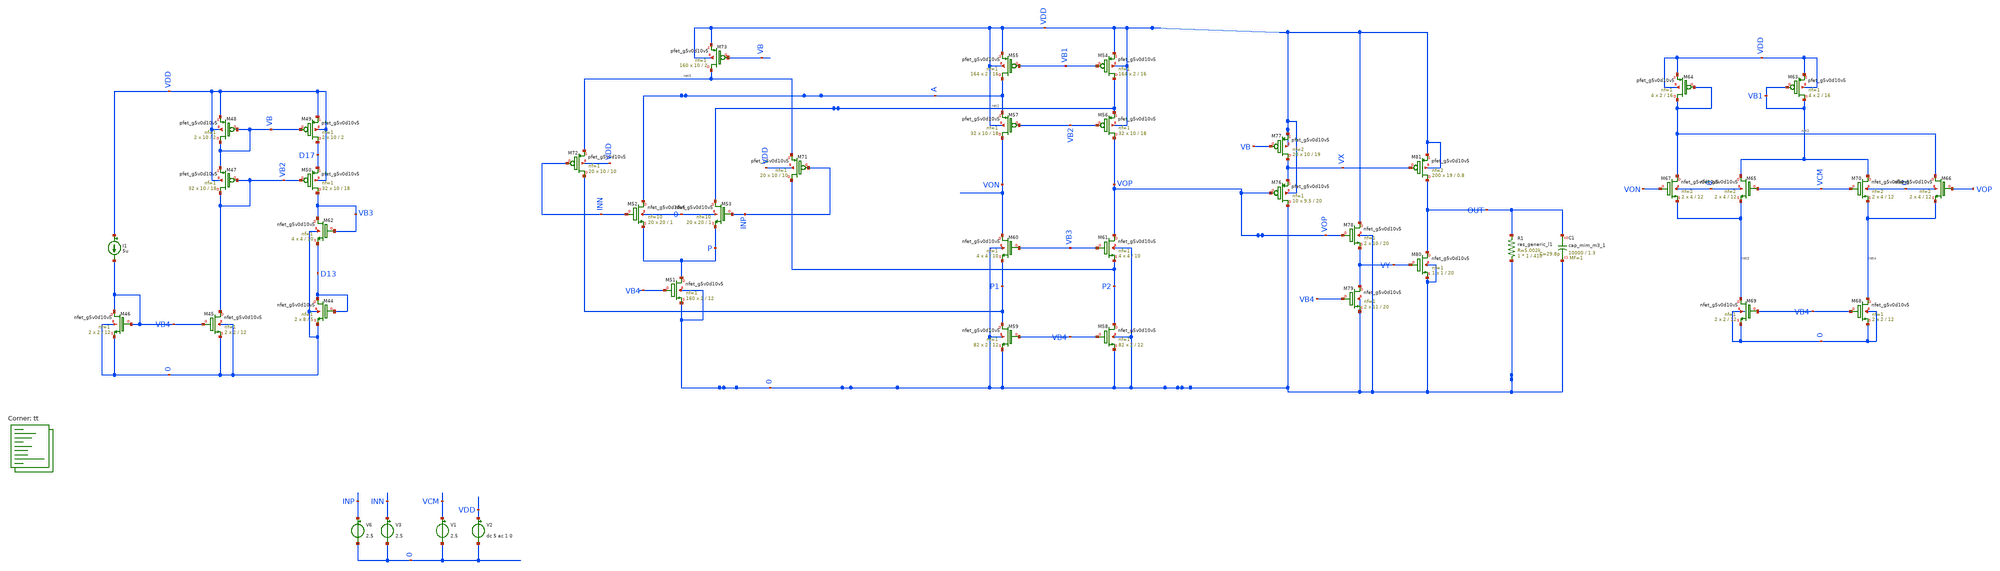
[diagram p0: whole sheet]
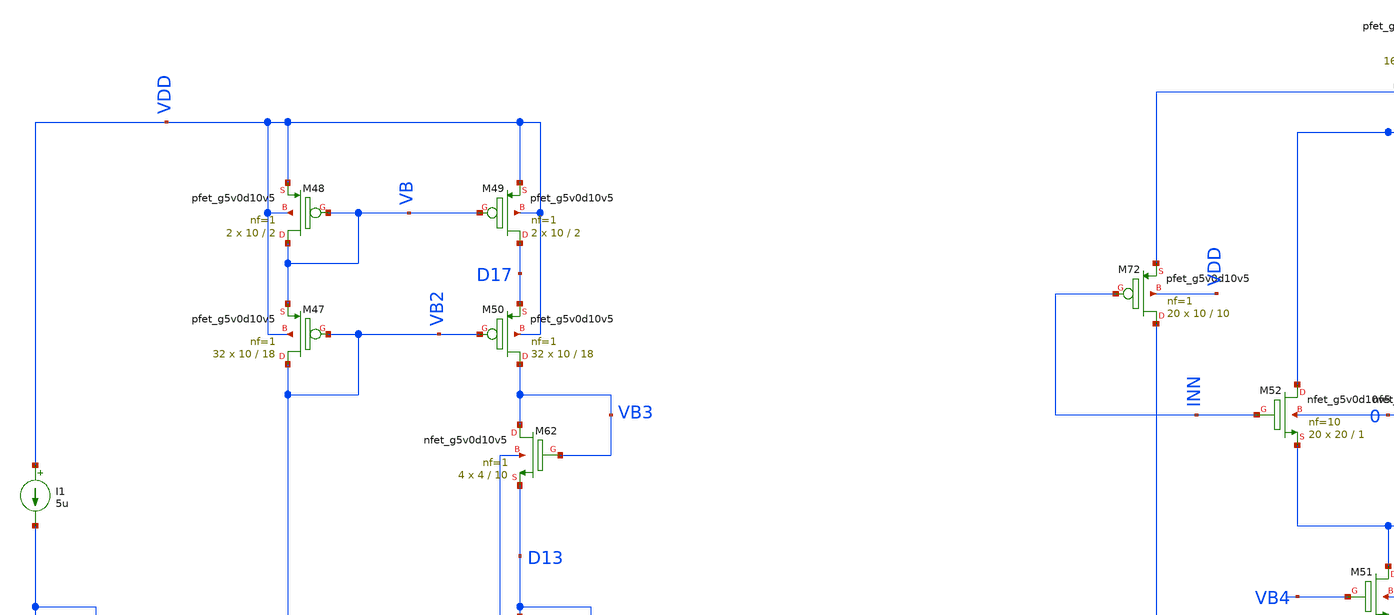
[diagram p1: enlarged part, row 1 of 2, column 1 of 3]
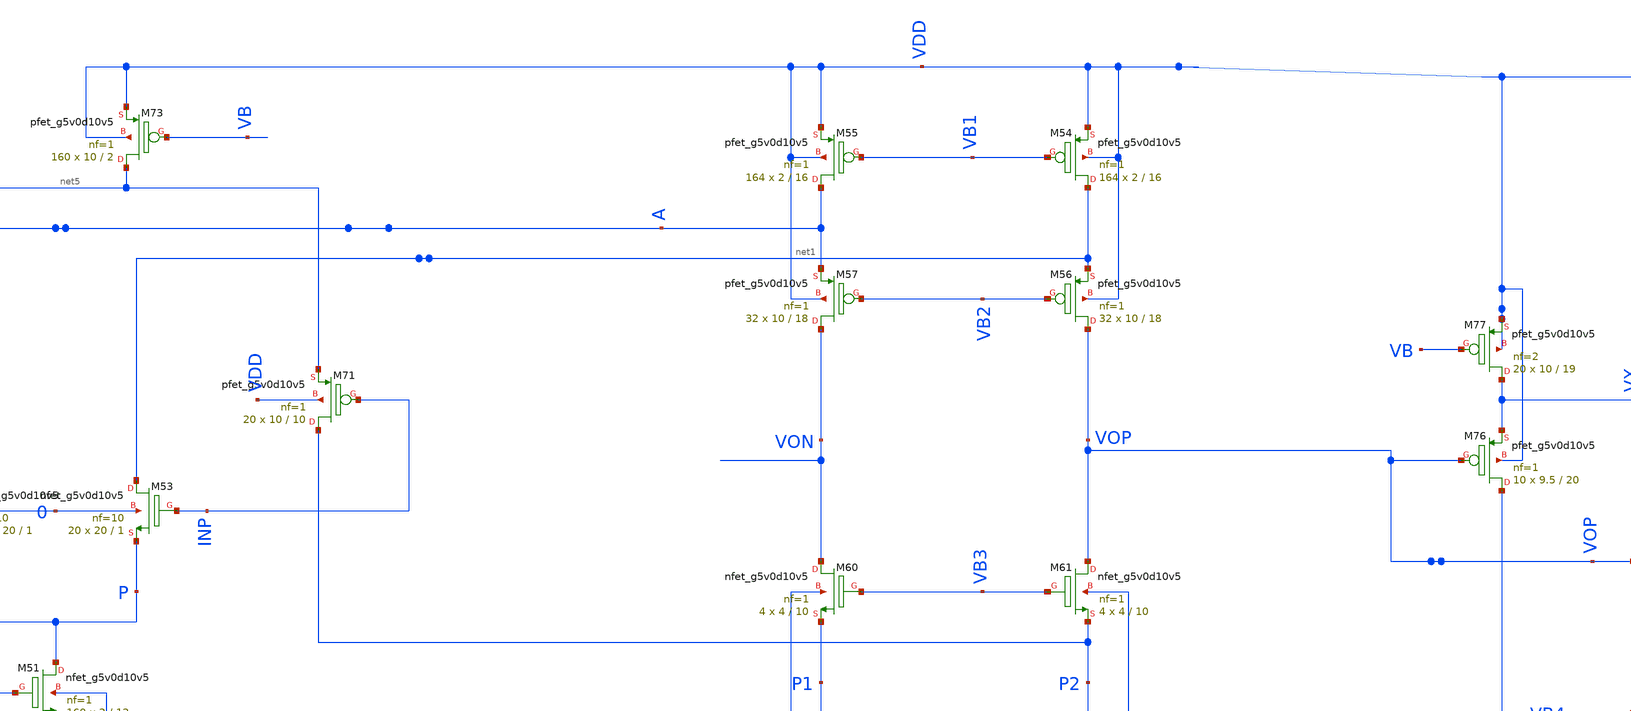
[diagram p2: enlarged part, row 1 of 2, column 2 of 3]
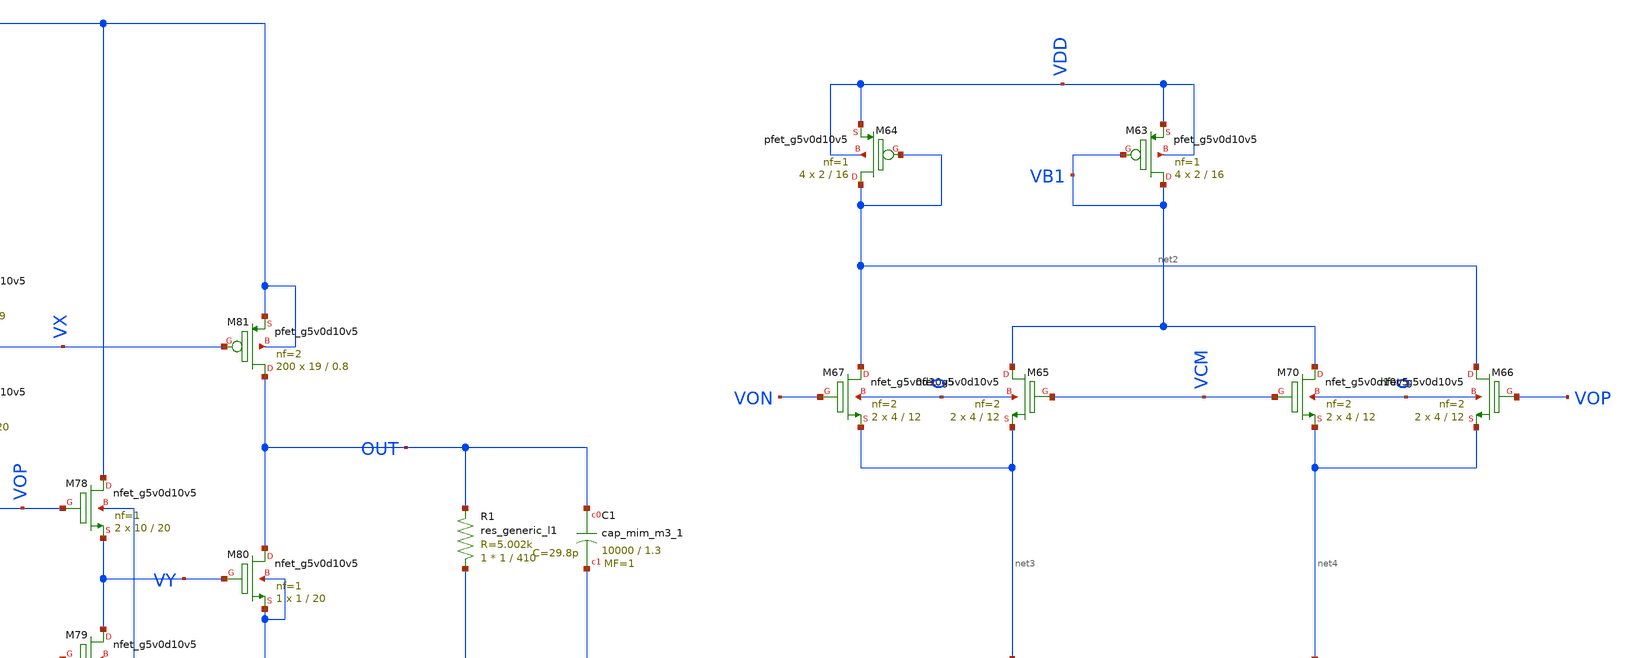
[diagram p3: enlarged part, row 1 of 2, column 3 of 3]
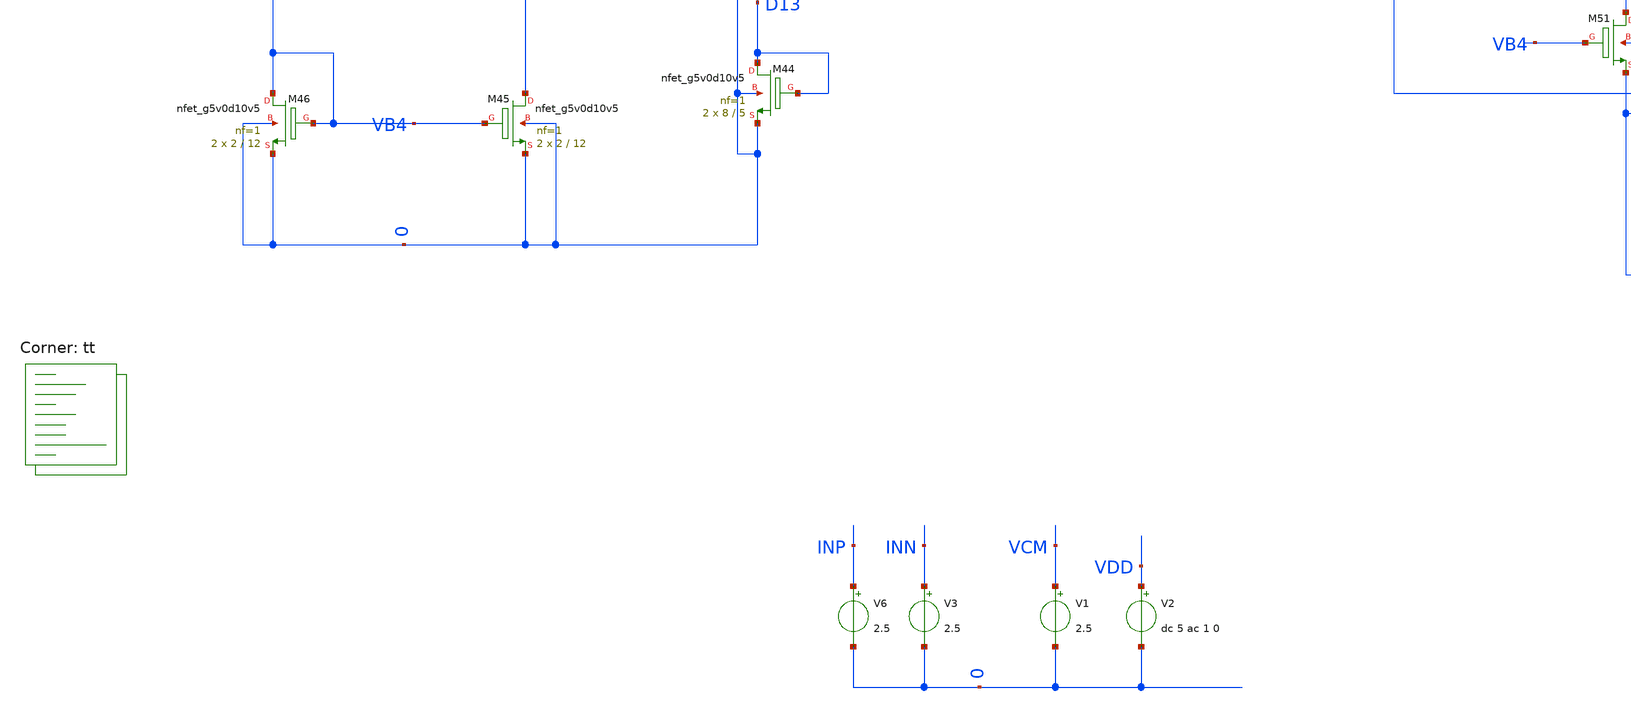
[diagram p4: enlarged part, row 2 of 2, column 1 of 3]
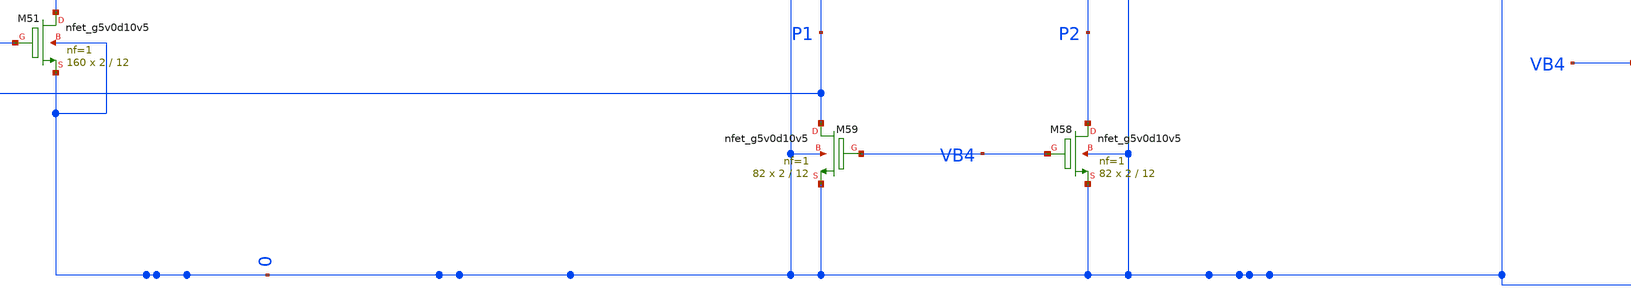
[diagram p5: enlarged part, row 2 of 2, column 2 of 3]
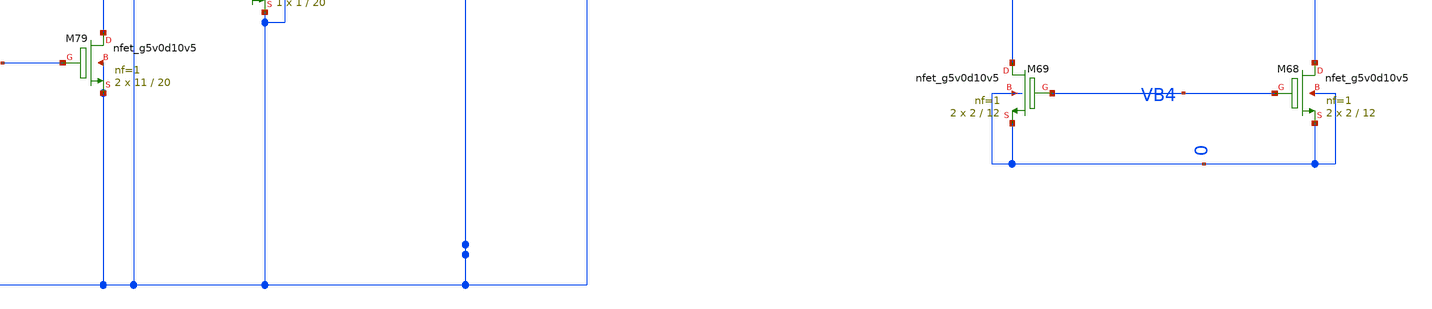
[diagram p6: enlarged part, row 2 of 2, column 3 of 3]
** sch_path: Xschem_UPDATE/tb_PSRR_MEAS_final.sch
**.subckt tb_PSRR_MEAS_final
V6 INP 0 2.5
V1 VCM 0 2.5
V2 VDD 0 dc 5 ac 1 0
V3 INN 0 2.5
I1 VDD VB4 5u
XM44 D13 D13 0 0 sky130_fd_pr__nfet_g5v0d10v5 L=5 W=8 nf=1 ad='int((nf+1)/2) * W/nf * 0.29' as='int((nf+2)/2) * W/nf * 0.29'
+ pd='2*int((nf+1)/2) * (W/nf + 0.29)' ps='2*int((nf+2)/2) * (W/nf + 0.29)' nrd='0.29 / W' nrs='0.29 / W'
+ sa=0 sb=0 sd=0 mult=2 m=2
XM45 VB2 VB4 0 0 sky130_fd_pr__nfet_g5v0d10v5 L=12 W=2 nf=1 ad='int((nf+1)/2) * W/nf * 0.29' as='int((nf+2)/2) * W/nf * 0.29'
+ pd='2*int((nf+1)/2) * (W/nf + 0.29)' ps='2*int((nf+2)/2) * (W/nf + 0.29)' nrd='0.29 / W' nrs='0.29 / W'
+ sa=0 sb=0 sd=0 mult=2 m=2
XM46 VB4 VB4 0 0 sky130_fd_pr__nfet_g5v0d10v5 L=12 W=2 nf=1 ad='int((nf+1)/2) * W/nf * 0.29' as='int((nf+2)/2) * W/nf * 0.29'
+ pd='2*int((nf+1)/2) * (W/nf + 0.29)' ps='2*int((nf+2)/2) * (W/nf + 0.29)' nrd='0.29 / W' nrs='0.29 / W'
+ sa=0 sb=0 sd=0 mult=2 m=2
XM47 VB2 VB2 VB VDD sky130_fd_pr__pfet_g5v0d10v5 L=18 W=10 nf=1 ad='int((nf+1)/2) * W/nf * 0.29' as='int((nf+2)/2) * W/nf * 0.29'
+ pd='2*int((nf+1)/2) * (W/nf + 0.29)' ps='2*int((nf+2)/2) * (W/nf + 0.29)' nrd='0.29 / W' nrs='0.29 / W'
+ sa=0 sb=0 sd=0 mult=32 m=32
XM48 VB VB VDD VDD sky130_fd_pr__pfet_g5v0d10v5 L=2 W=10 nf=1 ad='int((nf+1)/2) * W/nf * 0.29' as='int((nf+2)/2) * W/nf * 0.29'
+ pd='2*int((nf+1)/2) * (W/nf + 0.29)' ps='2*int((nf+2)/2) * (W/nf + 0.29)' nrd='0.29 / W' nrs='0.29 / W'
+ sa=0 sb=0 sd=0 mult=2 m=2
XM49 D17 VB VDD VDD sky130_fd_pr__pfet_g5v0d10v5 L=2 W=10 nf=1 ad='int((nf+1)/2) * W/nf * 0.29' as='int((nf+2)/2) * W/nf * 0.29'
+ pd='2*int((nf+1)/2) * (W/nf + 0.29)' ps='2*int((nf+2)/2) * (W/nf + 0.29)' nrd='0.29 / W' nrs='0.29 / W'
+ sa=0 sb=0 sd=0 mult=2 m=2
XM50 VB3 VB2 D17 VDD sky130_fd_pr__pfet_g5v0d10v5 L=18 W=10 nf=1 ad='int((nf+1)/2) * W/nf * 0.29' as='int((nf+2)/2) * W/nf * 0.29'
+ pd='2*int((nf+1)/2) * (W/nf + 0.29)' ps='2*int((nf+2)/2) * (W/nf + 0.29)' nrd='0.29 / W' nrs='0.29 / W'
+ sa=0 sb=0 sd=0 mult=32 m=32
XM51 P VB4 0 0 sky130_fd_pr__nfet_g5v0d10v5 L=12 W=2 nf=1 ad='int((nf+1)/2) * W/nf * 0.29' as='int((nf+2)/2) * W/nf * 0.29'
+ pd='2*int((nf+1)/2) * (W/nf + 0.29)' ps='2*int((nf+2)/2) * (W/nf + 0.29)' nrd='0.29 / W' nrs='0.29 / W'
+ sa=0 sb=0 sd=0 mult=160 m=160
XM52 A INN P 0 sky130_fd_pr__nfet_g5v0d10v5 L=1 W=20 nf=10 ad='int((nf+1)/2) * W/nf * 0.29' as='int((nf+2)/2) * W/nf * 0.29'
+ pd='2*int((nf+1)/2) * (W/nf + 0.29)' ps='2*int((nf+2)/2) * (W/nf + 0.29)' nrd='0.29 / W' nrs='0.29 / W'
+ sa=0 sb=0 sd=0 mult=20 m=20
XM53 net1 INP P 0 sky130_fd_pr__nfet_g5v0d10v5 L=1 W=20 nf=10 ad='int((nf+1)/2) * W/nf * 0.29' as='int((nf+2)/2) * W/nf * 0.29'
+ pd='2*int((nf+1)/2) * (W/nf + 0.29)' ps='2*int((nf+2)/2) * (W/nf + 0.29)' nrd='0.29 / W' nrs='0.29 / W'
+ sa=0 sb=0 sd=0 mult=20 m=20
XM54 net1 VB1 VDD VDD sky130_fd_pr__pfet_g5v0d10v5 L=16 W=2 nf=1 ad='int((nf+1)/2) * W/nf * 0.29' as='int((nf+2)/2) * W/nf * 0.29'
+ pd='2*int((nf+1)/2) * (W/nf + 0.29)' ps='2*int((nf+2)/2) * (W/nf + 0.29)' nrd='0.29 / W' nrs='0.29 / W'
+ sa=0 sb=0 sd=0 mult=164 m=164
XM55 A VB1 VDD VDD sky130_fd_pr__pfet_g5v0d10v5 L=16 W=2 nf=1 ad='int((nf+1)/2) * W/nf * 0.29' as='int((nf+2)/2) * W/nf * 0.29'
+ pd='2*int((nf+1)/2) * (W/nf + 0.29)' ps='2*int((nf+2)/2) * (W/nf + 0.29)' nrd='0.29 / W' nrs='0.29 / W'
+ sa=0 sb=0 sd=0 mult=164 m=164
XM56 VOP VB2 net1 VDD sky130_fd_pr__pfet_g5v0d10v5 L=18 W=10 nf=1 ad='int((nf+1)/2) * W/nf * 0.29' as='int((nf+2)/2) * W/nf * 0.29'
+ pd='2*int((nf+1)/2) * (W/nf + 0.29)' ps='2*int((nf+2)/2) * (W/nf + 0.29)' nrd='0.29 / W' nrs='0.29 / W'
+ sa=0 sb=0 sd=0 mult=32 m=32
XM57 VON VB2 A VDD sky130_fd_pr__pfet_g5v0d10v5 L=18 W=10 nf=1 ad='int((nf+1)/2) * W/nf * 0.29' as='int((nf+2)/2) * W/nf * 0.29'
+ pd='2*int((nf+1)/2) * (W/nf + 0.29)' ps='2*int((nf+2)/2) * (W/nf + 0.29)' nrd='0.29 / W' nrs='0.29 / W'
+ sa=0 sb=0 sd=0 mult=32 m=32
XM58 P2 VB4 0 0 sky130_fd_pr__nfet_g5v0d10v5 L=12 W=2 nf=1 ad='int((nf+1)/2) * W/nf * 0.29' as='int((nf+2)/2) * W/nf * 0.29'
+ pd='2*int((nf+1)/2) * (W/nf + 0.29)' ps='2*int((nf+2)/2) * (W/nf + 0.29)' nrd='0.29 / W' nrs='0.29 / W'
+ sa=0 sb=0 sd=0 mult=82 m=82
XM59 P1 VB4 0 0 sky130_fd_pr__nfet_g5v0d10v5 L=12 W=2 nf=1 ad='int((nf+1)/2) * W/nf * 0.29' as='int((nf+2)/2) * W/nf * 0.29'
+ pd='2*int((nf+1)/2) * (W/nf + 0.29)' ps='2*int((nf+2)/2) * (W/nf + 0.29)' nrd='0.29 / W' nrs='0.29 / W'
+ sa=0 sb=0 sd=0 mult=82 m=82
XM60 VON VB3 P1 0 sky130_fd_pr__nfet_g5v0d10v5 L=10 W=4 nf=1 ad='int((nf+1)/2) * W/nf * 0.29' as='int((nf+2)/2) * W/nf * 0.29'
+ pd='2*int((nf+1)/2) * (W/nf + 0.29)' ps='2*int((nf+2)/2) * (W/nf + 0.29)' nrd='0.29 / W' nrs='0.29 / W'
+ sa=0 sb=0 sd=0 mult=4 m=4
XM61 VOP VB3 P2 0 sky130_fd_pr__nfet_g5v0d10v5 L=10 W=4 nf=1 ad='int((nf+1)/2) * W/nf * 0.29' as='int((nf+2)/2) * W/nf * 0.29'
+ pd='2*int((nf+1)/2) * (W/nf + 0.29)' ps='2*int((nf+2)/2) * (W/nf + 0.29)' nrd='0.29 / W' nrs='0.29 / W'
+ sa=0 sb=0 sd=0 mult=4 m=4
XM62 VB3 VB3 D13 0 sky130_fd_pr__nfet_g5v0d10v5 L=10 W=4 nf=1 ad='int((nf+1)/2) * W/nf * 0.29' as='int((nf+2)/2) * W/nf * 0.29'
+ pd='2*int((nf+1)/2) * (W/nf + 0.29)' ps='2*int((nf+2)/2) * (W/nf + 0.29)' nrd='0.29 / W' nrs='0.29 / W'
+ sa=0 sb=0 sd=0 mult=4 m=4
XM63 VB1 VB1 VDD VDD sky130_fd_pr__pfet_g5v0d10v5 L=16 W=2 nf=1 ad='int((nf+1)/2) * W/nf * 0.29' as='int((nf+2)/2) * W/nf * 0.29'
+ pd='2*int((nf+1)/2) * (W/nf + 0.29)' ps='2*int((nf+2)/2) * (W/nf + 0.29)' nrd='0.29 / W' nrs='0.29 / W'
+ sa=0 sb=0 sd=0 mult=4 m=4
XM64 net2 net2 VDD VDD sky130_fd_pr__pfet_g5v0d10v5 L=16 W=2 nf=1 ad='int((nf+1)/2) * W/nf * 0.29' as='int((nf+2)/2) * W/nf * 0.29'
+ pd='2*int((nf+1)/2) * (W/nf + 0.29)' ps='2*int((nf+2)/2) * (W/nf + 0.29)' nrd='0.29 / W' nrs='0.29 / W'
+ sa=0 sb=0 sd=0 mult=4 m=4
XM65 VB1 VCM net3 0 sky130_fd_pr__nfet_g5v0d10v5 L=12 W=4 nf=2 ad='int((nf+1)/2) * W/nf * 0.29' as='int((nf+2)/2) * W/nf * 0.29'
+ pd='2*int((nf+1)/2) * (W/nf + 0.29)' ps='2*int((nf+2)/2) * (W/nf + 0.29)' nrd='0.29 / W' nrs='0.29 / W'
+ sa=0 sb=0 sd=0 mult=2 m=2
XM66 net2 VOP net4 0 sky130_fd_pr__nfet_g5v0d10v5 L=12 W=4 nf=2 ad='int((nf+1)/2) * W/nf * 0.29' as='int((nf+2)/2) * W/nf * 0.29'
+ pd='2*int((nf+1)/2) * (W/nf + 0.29)' ps='2*int((nf+2)/2) * (W/nf + 0.29)' nrd='0.29 / W' nrs='0.29 / W'
+ sa=0 sb=0 sd=0 mult=2 m=2
XM67 net2 VON net3 0 sky130_fd_pr__nfet_g5v0d10v5 L=12 W=4 nf=2 ad='int((nf+1)/2) * W/nf * 0.29' as='int((nf+2)/2) * W/nf * 0.29'
+ pd='2*int((nf+1)/2) * (W/nf + 0.29)' ps='2*int((nf+2)/2) * (W/nf + 0.29)' nrd='0.29 / W' nrs='0.29 / W'
+ sa=0 sb=0 sd=0 mult=2 m=2
XM68 net4 VB4 0 0 sky130_fd_pr__nfet_g5v0d10v5 L=12 W=2 nf=1 ad='int((nf+1)/2) * W/nf * 0.29' as='int((nf+2)/2) * W/nf * 0.29'
+ pd='2*int((nf+1)/2) * (W/nf + 0.29)' ps='2*int((nf+2)/2) * (W/nf + 0.29)' nrd='0.29 / W' nrs='0.29 / W'
+ sa=0 sb=0 sd=0 mult=2 m=2
XM69 net3 VB4 0 0 sky130_fd_pr__nfet_g5v0d10v5 L=12 W=2 nf=1 ad='int((nf+1)/2) * W/nf * 0.29' as='int((nf+2)/2) * W/nf * 0.29'
+ pd='2*int((nf+1)/2) * (W/nf + 0.29)' ps='2*int((nf+2)/2) * (W/nf + 0.29)' nrd='0.29 / W' nrs='0.29 / W'
+ sa=0 sb=0 sd=0 mult=2 m=2
XM70 VB1 VCM net4 0 sky130_fd_pr__nfet_g5v0d10v5 L=12 W=4 nf=2 ad='int((nf+1)/2) * W/nf * 0.29' as='int((nf+2)/2) * W/nf * 0.29'
+ pd='2*int((nf+1)/2) * (W/nf + 0.29)' ps='2*int((nf+2)/2) * (W/nf + 0.29)' nrd='0.29 / W' nrs='0.29 / W'
+ sa=0 sb=0 sd=0 mult=2 m=2
XM71 P2 INP net5 VDD sky130_fd_pr__pfet_g5v0d10v5 L=10 W=10 nf=1 ad='int((nf+1)/2) * W/nf * 0.29' as='int((nf+2)/2) * W/nf * 0.29'
+ pd='2*int((nf+1)/2) * (W/nf + 0.29)' ps='2*int((nf+2)/2) * (W/nf + 0.29)' nrd='0.29 / W' nrs='0.29 / W'
+ sa=0 sb=0 sd=0 mult=20 m=20
XM72 P1 INN net5 VDD sky130_fd_pr__pfet_g5v0d10v5 L=10 W=10 nf=1 ad='int((nf+1)/2) * W/nf * 0.29' as='int((nf+2)/2) * W/nf * 0.29'
+ pd='2*int((nf+1)/2) * (W/nf + 0.29)' ps='2*int((nf+2)/2) * (W/nf + 0.29)' nrd='0.29 / W' nrs='0.29 / W'
+ sa=0 sb=0 sd=0 mult=20 m=20
XM73 net5 VB VDD VDD sky130_fd_pr__pfet_g5v0d10v5 L=2 W=10 nf=1 ad='int((nf+1)/2) * W/nf * 0.29' as='int((nf+2)/2) * W/nf * 0.29'
+ pd='2*int((nf+1)/2) * (W/nf + 0.29)' ps='2*int((nf+2)/2) * (W/nf + 0.29)' nrd='0.29 / W' nrs='0.29 / W'
+ sa=0 sb=0 sd=0 mult=160 m=160
XM76 0 VOP VX VDD sky130_fd_pr__pfet_g5v0d10v5 L=20 W=9.5 nf=1 ad='int((nf+1)/2) * W/nf * 0.29' as='int((nf+2)/2) * W/nf * 0.29'
+ pd='2*int((nf+1)/2) * (W/nf + 0.29)' ps='2*int((nf+2)/2) * (W/nf + 0.29)' nrd='0.29 / W' nrs='0.29 / W'
+ sa=0 sb=0 sd=0 mult=10 m=10
XM77 VX VB VDD VDD sky130_fd_pr__pfet_g5v0d10v5 L=19 W=10 nf=2 ad='int((nf+1)/2) * W/nf * 0.29' as='int((nf+2)/2) * W/nf * 0.29'
+ pd='2*int((nf+1)/2) * (W/nf + 0.29)' ps='2*int((nf+2)/2) * (W/nf + 0.29)' nrd='0.29 / W' nrs='0.29 / W'
+ sa=0 sb=0 sd=0 mult=20 m=20
XM78 VDD VOP VY 0 sky130_fd_pr__nfet_g5v0d10v5 L=20 W=10 nf=1 ad='int((nf+1)/2) * W/nf * 0.29' as='int((nf+2)/2) * W/nf * 0.29'
+ pd='2*int((nf+1)/2) * (W/nf + 0.29)' ps='2*int((nf+2)/2) * (W/nf + 0.29)' nrd='0.29 / W' nrs='0.29 / W'
+ sa=0 sb=0 sd=0 mult=2 m=2
XM79 VY VB4 0 0 sky130_fd_pr__nfet_g5v0d10v5 L=20 W=11 nf=1 ad='int((nf+1)/2) * W/nf * 0.29' as='int((nf+2)/2) * W/nf * 0.29'
+ pd='2*int((nf+1)/2) * (W/nf + 0.29)' ps='2*int((nf+2)/2) * (W/nf + 0.29)' nrd='0.29 / W' nrs='0.29 / W'
+ sa=0 sb=0 sd=0 mult=2 m=2
XM80 OUT VY 0 0 sky130_fd_pr__nfet_g5v0d10v5 L=20 W=1 nf=1 ad='int((nf+1)/2) * W/nf * 0.29' as='int((nf+2)/2) * W/nf * 0.29'
+ pd='2*int((nf+1)/2) * (W/nf + 0.29)' ps='2*int((nf+2)/2) * (W/nf + 0.29)' nrd='0.29 / W' nrs='0.29 / W'
+ sa=0 sb=0 sd=0 mult=1 m=1
XM81 OUT VX VDD VDD sky130_fd_pr__pfet_g5v0d10v5 L=0.8 W=19 nf=2 ad='int((nf+1)/2) * W/nf * 0.29' as='int((nf+2)/2) * W/nf * 0.29'
+ pd='2*int((nf+1)/2) * (W/nf + 0.29)' ps='2*int((nf+2)/2) * (W/nf + 0.29)' nrd='0.29 / W' nrs='0.29 / W'
+ sa=0 sb=0 sd=0 mult=200 m=200
XC1 OUT 0 sky130_fd_pr__cap_mim_m3_1 W=10000 L=1.3 MF=1 m=1
R1 0 OUT sky130_fd_pr__res_generic_l1 W=1 L=410 m=1
**** begin user architecture code

* this option enables mos model bin
* selection based on W/NF instead of W
.option wnflag=1
.option savecurrents

.control
save all
save @m.xm15.msky130_fd_pr__pfet_g5v0d10v5[vth]
save @m.xm15.msky130_fd_pr__pfet_g5v0d10v5[gm]
save @m.xm9.msky130_fd_pr__pfet_g5v0d10v5[vth]
save @m.xm9.msky130_fd_pr__pfet_g5v0d10v5[gm]
save @m.xm8.msky130_fd_pr__pfet_g5v0d10v5[vth]
save @m.xm8.msky130_fd_pr__pfet_g5v0d10v5[gm]
save @m.xm20.msky130_fd_pr__pfet_g5v0d10v5[vth]
save @m.xm20.msky130_fd_pr__pfet_g5v0d10v5[gm]
save @m.xm7.msky130_fd_pr__pfet_g5v0d10v5[vth]
save @m.xm7.msky130_fd_pr__pfet_g5v0d10v5[gm]
save @m.xm10.msky130_fd_pr__nfet_g5v0d10v5[gm]
save @m.xm10.msky130_fd_pr__nfet_g5v0d10v5[vth]
save @m.xm14.msky130_fd_pr__pfet_g5v0d10v5[gm]
save @m.xm14.msky130_fd_pr__pfet_g5v0d10v5[vth]
save @m.xm16.msky130_fd_pr__pfet_g5v0d10v5[gm]
save @m.xm16.msky130_fd_pr__pfet_g5v0d10v5[vth]
save @m.xm17.msky130_fd_pr__pfet_g5v0d10v5[gm]
save @m.xm17.msky130_fd_pr__pfet_g5v0d10v5[vth]
save @m.xm13.msky130_fd_pr__nfet_g5v0d10v5[gm]
save @m.xm13.msky130_fd_pr__nfet_g5v0d10v5[vth]
save @m.xm12.msky130_fd_pr__nfet_g5v0d10v5[vth]
save @m.xm18.msky130_fd_pr__nfet_g5v0d10v5[vth]
*folded
save @m.xm2.msky130_fd_pr__nfet_g5v0d10v5[vth]
save @m.xm11.msky130_fd_pr__nfet_g5v0d10v5[vth]
save @m.xm1.msky130_fd_pr__nfet_g5v0d10v5[vth]
save @m.xm5.msky130_fd_pr__nfet_g5v0d10v5[vth]
save @m.xm6.msky130_fd_pr__nfet_g5v0d10v5[vth]
save @m.xm4.msky130_fd_pr__nfet_g5v0d10v5[vth]
save @m.xm3.msky130_fd_pr__nfet_g5v0d10v5[vth]
save @m.xm7.msky130_fd_pr__pfet_g5v0d10v5[vth]
save @m.xm8.msky130_fd_pr__pfet_g5v0d10v5[vth]
save @m.xm9.msky130_fd_pr__pfet_g5v0d10v5[vth]
save @m.xm20.msky130_fd_pr__pfet_g5v0d10v5[vth]
*CMFB
save @m.xm21.msky130_fd_pr__pfet_g5v0d10v5[vth]
save @m.xm19.msky130_fd_pr__pfet_g5v0d10v5[vth]
save @m.xm22.msky130_fd_pr__nfet_g5v0d10v5[vth]
save @m.xm23.msky130_fd_pr__nfet_g5v0d10v5[vth]
save @m.xm25.msky130_fd_pr__nfet_g5v0d10v5[vth]
save @m.xm27.msky130_fd_pr__nfet_g5v0d10v5[vth]
save @m.xm26.msky130_fd_pr__nfet_g5v0d10v5[vth]
save @m.xm24.msky130_fd_pr__nfet_g5v0d10v5[vth]
save current


write Folded_Buffer.raw

op
print VON VOP VB2 VB VX OUT VY
*print @m.xm18.msky130_fd_pr__nfet_g5v0d10v5
*print @m.xm12.msky130_fd_pr__nfet_g5v0d10v5
*print @m.xm13.msky130_fd_pr__nfet_g5v0d10v5
*print @m.xm10.msky130_fd_pr__nfet_g5v0d10v5
*print @m.xm14.msky130_fd_pr__pfet_g5v0d10v5
*print @m.xm17.msky130_fd_pr__pfet_g5v0d10v5
*print @m.xm15.msky130_fd_pr__pfet_g5v0d10v5
*print @m.xm16.msky130_fd_pr__pfet_g5v0d10v5
*Folded cascode
*print @m.xm9.msky130_fd_pr__pfet_g5v0d10v5
*print @m.xm8.msky130_fd_pr__pfet_g5v0d10v5
*print @m.xm5.msky130_fd_pr__nfet_g5v0d10v5
*print @m.xm4.msky130_fd_pr__nfet_g5v0d10v5
*print @m.xm1.msky130_fd_pr__nfet_g5v0d10v5
*print @m.xm2.msky130_fd_pr__nfet_g5v0d10v5
*print @m.xm11.msky130_fd_pr__nfet_g5v0d10v5
*CMFB
*print @m.xm23.msky130_fd_pr__nfet_g5v0d10v5
*print @m.xm24.msky130_fd_pr__nfet_g5v0d10v5
*print @m.xm25.msky130_fd_pr__nfet_g5v0d10v5
*print @m.xm22.msky130_fd_pr__nfet_g5v0d10v5
print @m.xm77.msky130_fd_pr__pfet_g5v0d10v5
print @m.xm76.msky130_fd_pr__pfet_g5v0d10v5
print @m.xm78.msky130_fd_pr__nfet_g5v0d10v5
print @m.xm79.msky130_fd_pr__nfet_g5v0d10v5
print @m.xm80.msky130_fd_pr__nfet_g5v0d10v5
print @m.xm81.msky130_fd_pr__pfet_g5v0d10v5
write Folded_Buffer.raw
ac dec 10 1 1e9
  remzerovec
  write tb_PSRR_MEAS_final.raw
quit 0
.endc


.lib $::SKYWATER_MODELS/sky130.lib.spice tt
**** end user architecture code
**.ends
.end
